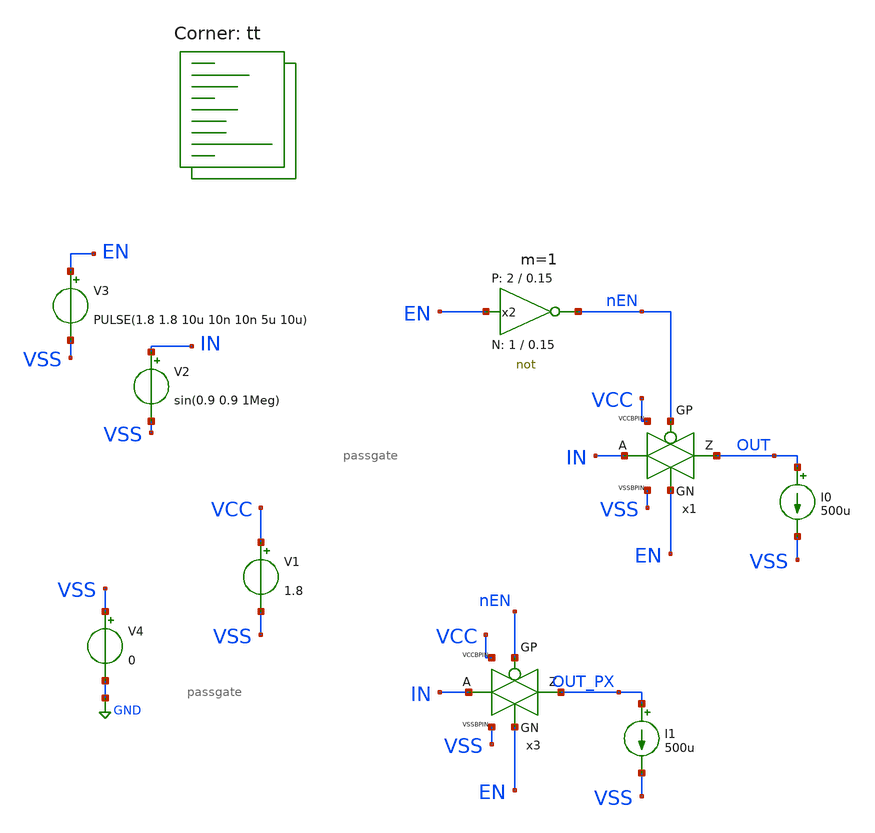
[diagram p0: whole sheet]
** sch_path: xschem/tb_passgaterdson.sch
* StefanSchippers/xschem_sky130/sky130_tests/not.sch:
* Copyright 2021 Stefan Frederik Schippers
* Licensed under the Apache License, Version 2.0 (the "License");
**.subckt tb_passgaterdson
x1 OUT IN nEN EN VSS VCC passgate
V1 VCC VSS 1.8
x2 nEN EN VCC VSS not W_N=1 L_N=0.15 W_P=2 L_P=0.15 m=1
V2 IN VSS sin(0.9 0.9 1Meg)
V3 EN VSS PULSE(1.8 1.8 10u 10n 10n 5u 10u)
V4 VSS GND 0
x3 OUT_PX IN nEN EN VSS VCC passgate_parax
I0 OUT VSS 500u
I1 OUT_PX VSS 500u
**** begin user architecture code
.lib $::SKYWATER_MODELS/sky130.lib.spice tt
**** end user architecture code
**.ends

* expanding   symbol:  passgate.sym # of pins=6
** sym_path: xschem/passgate.sym
** sch_path: xschem/passgate.sch
.subckt passgate Z A GP GN VSSBPIN VCCBPIN
*.ipin GN
*.ipin VCCBPIN
*.ipin VSSBPIN
*.ipin GP
*.iopin A
*.iopin Z
XM1 Z GN A VSSBPIN sky130_fd_pr__nfet_01v8_lvt L=0.35 W=8 nf=1 ad='int((nf+1)/2) * W/nf * 0.29' as='int((nf+2)/2) * W/nf * 0.29'
+ pd='2*int((nf+1)/2) * (W/nf + 0.29)' ps='2*int((nf+2)/2) * (W/nf + 0.29)' nrd='0.29 / W' nrs='0.29 / W'
+ sa=0 sb=0 sd=0 mult=2 m=2
XM3 Z GP A VCCBPIN sky130_fd_pr__pfet_01v8_lvt L=0.35 W=10 nf=1 ad='int((nf+1)/2) * W/nf * 0.29' as='int((nf+2)/2) * W/nf * 0.29'
+ pd='2*int((nf+1)/2) * (W/nf + 0.29)' ps='2*int((nf+2)/2) * (W/nf + 0.29)' nrd='0.29 / W' nrs='0.29 / W'
+ sa=0 sb=0 sd=0 mult=2 m=2
.ends


* expanding   symbol:  sky130_tests/not.sym # of pins=2
** sym_path: sky130_tests/not.sym
** sch_path: sky130_tests/not.sch
.subckt not y a VCCPIN VSSPIN     W_N=1 L_N=0.15 W_P=2 L_P=0.15
*.opin y
*.ipin a
XM1 DN a VSSPIN VSSPIN sky130_fd_pr__nfet_01v8 L=L_N W=W_N nf=1 ad='int((1 + 1)/2) * W_N / 1 * 0.29'
+ as='int((1 + 2)/2) * W_N / 1 * 0.29' pd='2*int((1 + 1)/2) * (W_N / 1 + 0.29)' ps='2*int((1 + 2)/2) * (W_N / 1 + 0.29)'
+ nrd='0.29 / W_N ' nrs='0.29 / W_N ' sa=0 sb=0 sd=0 mult=1 m=1
XM2 DP a VCCPIN VCCPIN sky130_fd_pr__pfet_01v8 L=L_P W=W_P nf=1 ad='int((nf+1)/2) * W/nf * 0.29' as='int((nf+2)/2) * W/nf * 0.29'
+ pd='2*int((nf+1)/2) * (W/nf + 0.29)' ps='2*int((nf+2)/2) * (W/nf + 0.29)' nrd='0.29 / W' nrs='0.29 / W'
+ sa=0 sb=0 sd=0 mult=1 m=1
Vmeas DP y 0
.save i(vmeas)
Vmeas1 y DN 0
.save i(vmeas1)
.save v(dp)
.save v(dn)
.ends


* expanding   symbol:  passgate_parax.sym # of pins=6
** sym_path: xschem/passgate.sym
.include [file normalize extracted/passgate_parax.spice]
.GLOBAL GND
**** begin user architecture code


* ngspice commands
* .options savecurrents

.control
dc V2 0 1.8 0.01

* plot (v(in) - v(out_px)) / 300u, (v(in) - v(out)) / 300u,
write tb_passgaterdson.raw
quit 0
.endc



**** end user architecture code
.end
